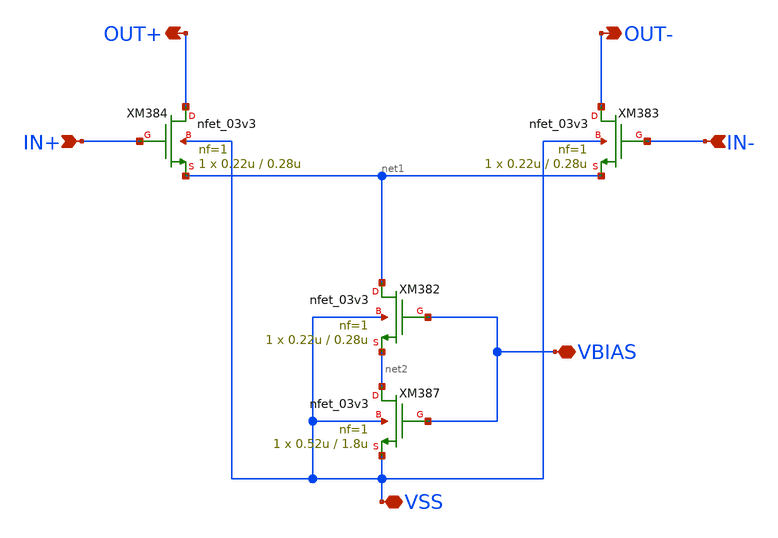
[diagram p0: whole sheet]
** sch_path: xschem/CS_Switch_2x.sch
**.subckt CS_Switch_2x IN+ IN- OUT- OUT+ VBIAS VSS
*.ipin IN+
*.ipin IN-
*.opin OUT-
*.opin OUT+
*.iopin VBIAS
*.iopin VSS
XM382 net1 VBIAS net2 VSS nfet_03v3 L=0.28u W=0.22u nf=1 ad='int((nf+1)/2) * W/nf * 0.18u' as='int((nf+2)/2) * W/nf * 0.18u'
+ pd='2*int((nf+1)/2) * (W/nf + 0.18u)' ps='2*int((nf+2)/2) * (W/nf + 0.18u)' nrd='0.18u / W' nrs='0.18u / W'
+ sa=0 sb=0 sd=0 m=1
XM383 OUT- IN- net1 VSS nfet_03v3 L=0.28u W=0.22u nf=1 ad='int((nf+1)/2) * W/nf * 0.18u' as='int((nf+2)/2) * W/nf * 0.18u'
+ pd='2*int((nf+1)/2) * (W/nf + 0.18u)' ps='2*int((nf+2)/2) * (W/nf + 0.18u)' nrd='0.18u / W' nrs='0.18u / W'
+ sa=0 sb=0 sd=0 m=1
XM384 OUT+ IN+ net1 VSS nfet_03v3 L=0.28u W=0.22u nf=1 ad='int((nf+1)/2) * W/nf * 0.18u' as='int((nf+2)/2) * W/nf * 0.18u'
+ pd='2*int((nf+1)/2) * (W/nf + 0.18u)' ps='2*int((nf+2)/2) * (W/nf + 0.18u)' nrd='0.18u / W' nrs='0.18u / W'
+ sa=0 sb=0 sd=0 m=1
XM387 net2 VBIAS VSS VSS nfet_03v3 L=1.8u W=0.52u nf=1 ad='int((nf+1)/2) * W/nf * 0.18u' as='int((nf+2)/2) * W/nf * 0.18u'
+ pd='2*int((nf+1)/2) * (W/nf + 0.18u)' ps='2*int((nf+2)/2) * (W/nf + 0.18u)' nrd='0.18u / W' nrs='0.18u / W'
+ sa=0 sb=0 sd=0 m=1
**.ends
.end
